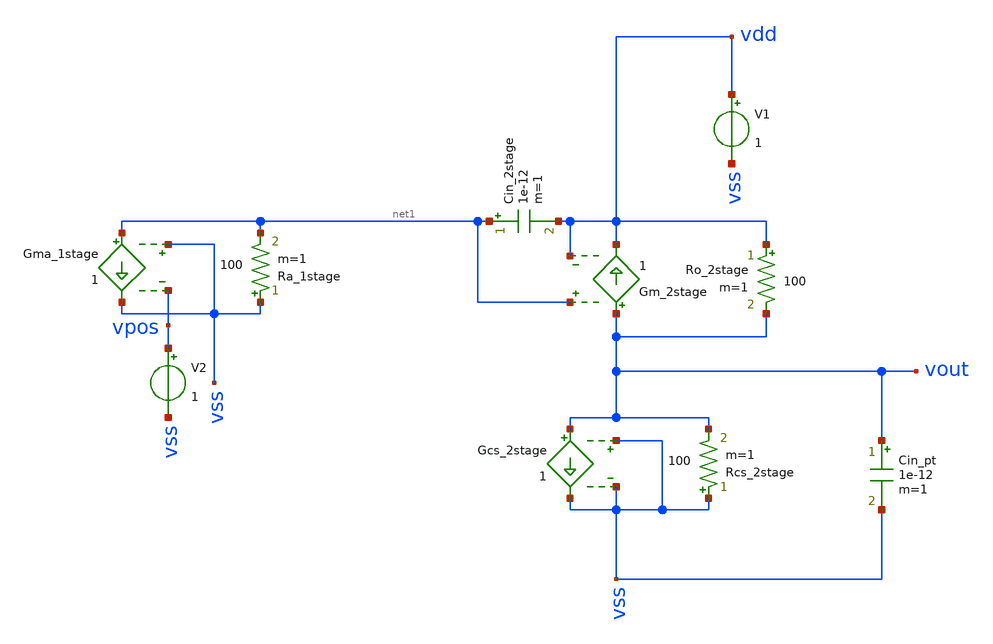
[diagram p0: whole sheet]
** sch_path: test-python/Tesis_notebooks/xschem/ota_2stage.sch
**.subckt ota_2stage
Ro_2stage vdd vout 100 m=1
Gm_2stage vout vdd net1 vdd 1
Gma_1stage net1 vss vss vpos 1
Ra_1stage vss net1 100 m=1
V1 vdd vss 1
Cin_2stage net1 vdd 1e-12 m=1
V2 vpos vss 1
Gcs_2stage vout vss vss vss 1
Rcs_2stage vss vout 100 m=1
Cin_pt vout vss 1e-12 m=1
**.ends
.end
